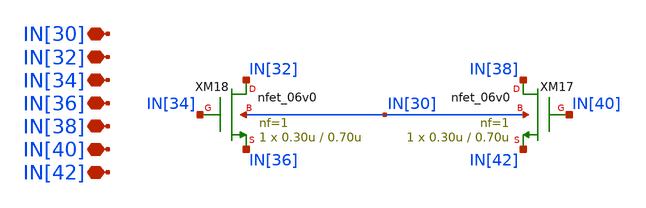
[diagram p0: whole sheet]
** sch_path: designs/libs/core_single-fet/nfet-pin/nfet-pin.sch
**.subckt nfet-pin IN[32] IN[30] IN[34] IN[36] IN[38] IN[40] IN[42]
*.iopin IN[32]
*.iopin IN[30]
*.iopin IN[34]
*.iopin IN[36]
*.iopin IN[38]
*.iopin IN[40]
*.iopin IN[42]
XM17 IN[38] IN[40] IN[42] IN[30] nfet_06v0 L=0.70u W=0.30u nf=1 ad='int((nf+1)/2) * W/nf * 0.18u' as='int((nf+2)/2) * W/nf * 0.18u'
+ pd='2*int((nf+1)/2) * (W/nf + 0.18u)' ps='2*int((nf+2)/2) * (W/nf + 0.18u)' nrd='0.18u / W' nrs='0.18u / W'
+ sa=0 sb=0 sd=0 m=1
XM18 IN[32] IN[34] IN[36] IN[30] nfet_06v0 L=0.70u W=0.30u nf=1 ad='int((nf+1)/2) * W/nf * 0.18u' as='int((nf+2)/2) * W/nf * 0.18u'
+ pd='2*int((nf+1)/2) * (W/nf + 0.18u)' ps='2*int((nf+2)/2) * (W/nf + 0.18u)' nrd='0.18u / W' nrs='0.18u / W'
+ sa=0 sb=0 sd=0 m=1
**.ends
.end
